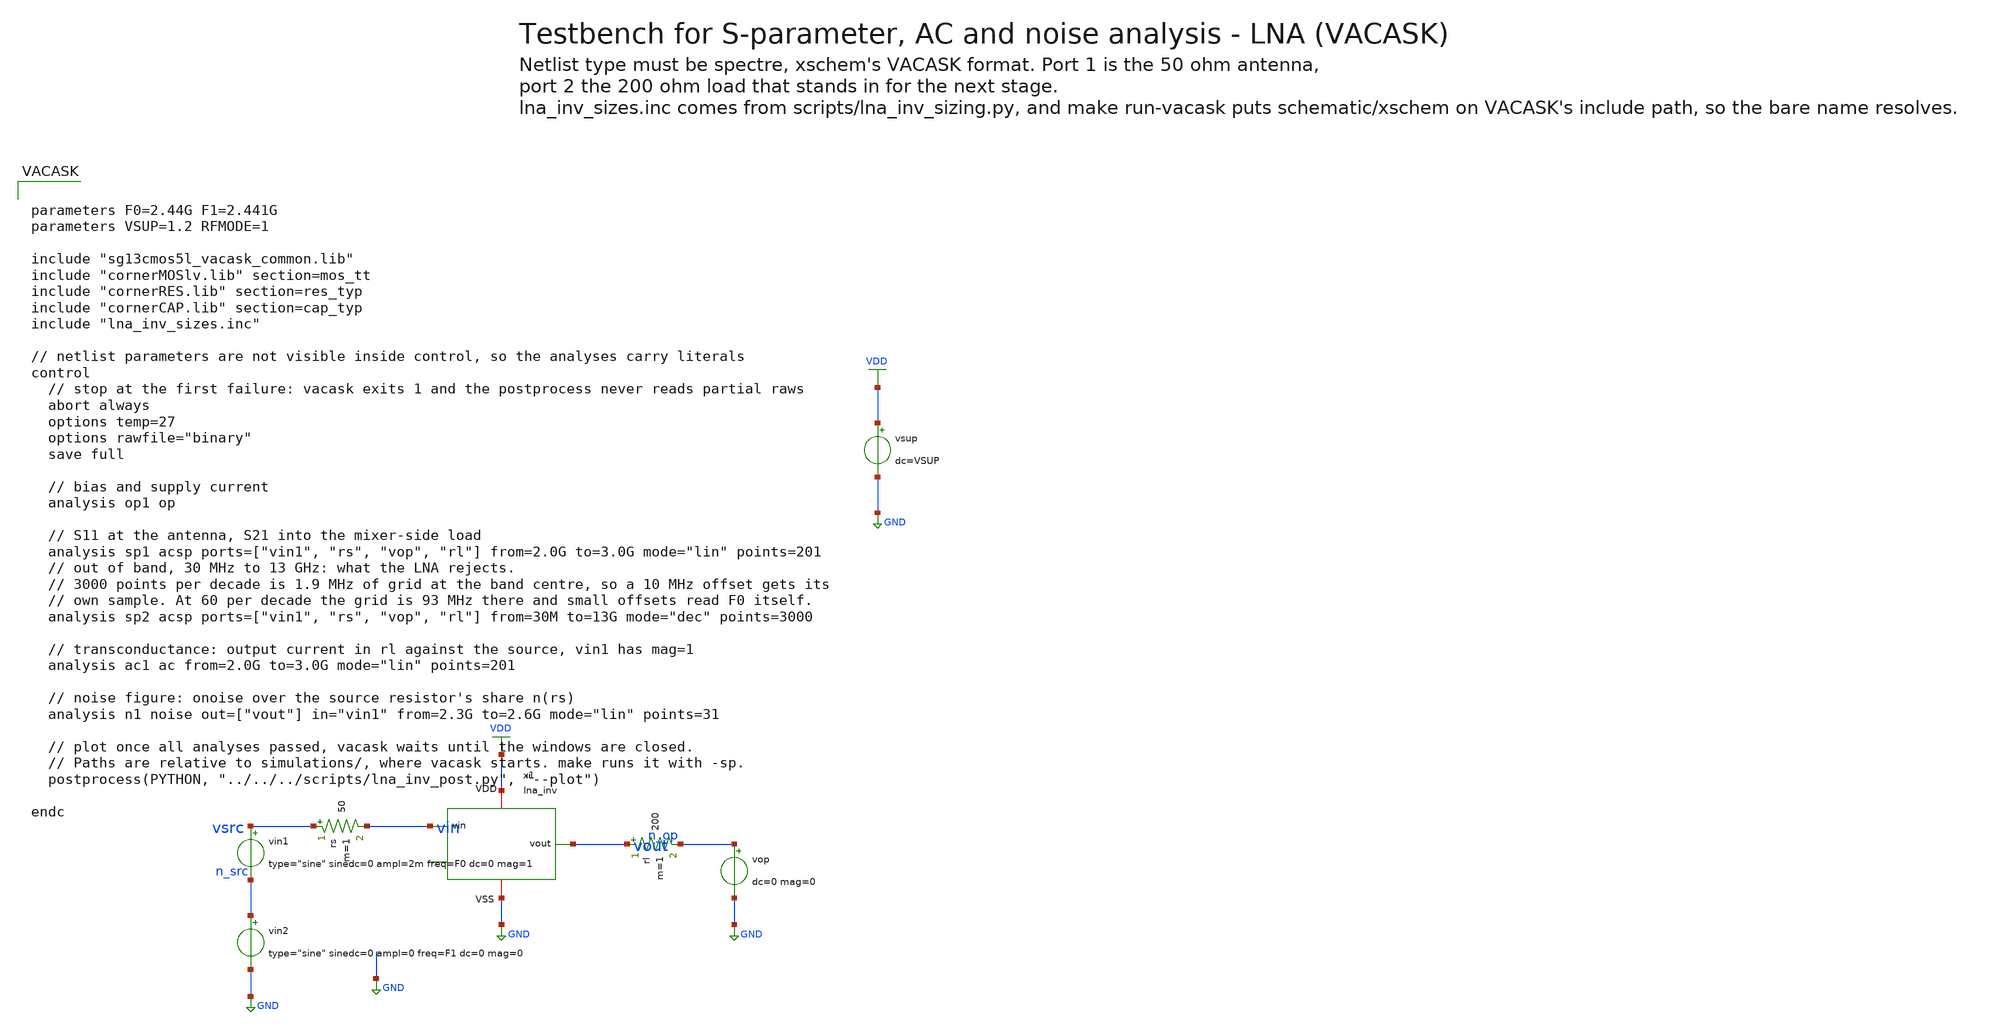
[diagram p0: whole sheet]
** sch_path: macros/lna_inv/testbenches/xschem/lna_inv_tb_sp.sch
**.subckt lna_inv_tb_sp
vin1 vsrc n_src type="sine" sinedc=0 ampl=2m freq=F0 dc=0 mag=1
vin2 n_src GND type="sine" sinedc=0 ampl=0 freq=F1 dc=0 mag=0
rs vsrc vin 50 m=1
x1 vin vout VDD GND lna_inv
rl vout n_op 200 m=1
vop n_op GND dc=0 mag=0
vsup VDD GND dc=VSUP
**** begin user architecture code


parameters F0=2.44G F1=2.441G
parameters VSUP=1.2 RFMODE=1

include "sg13cmos5l_vacask_common.lib"
include "cornerMOSlv.lib" section=mos_tt
include "cornerRES.lib" section=res_typ
include "cornerCAP.lib" section=cap_typ
include "lna_inv_sizes.inc"

// netlist parameters are not visible inside control, so the analyses carry literals
control
  // stop at the first failure: vacask exits 1 and the postprocess never reads partial raws
  abort always
  options temp=27
  options rawfile="binary"
  save full

  // bias and supply current
  analysis op1 op

  // S11 at the antenna, S21 into the mixer-side load
  analysis sp1 acsp ports=["vin1", "rs", "vop", "rl"] from=2.0G to=3.0G mode="lin" points=201
  // out of band, 30 MHz to 13 GHz: what the LNA rejects.
  // 3000 points per decade is 1.9 MHz of grid at the band centre, so a 10 MHz offset gets its
  // own sample. At 60 per decade the grid is 93 MHz there and small offsets read F0 itself.
  analysis sp2 acsp ports=["vin1", "rs", "vop", "rl"] from=30M to=13G mode="dec" points=3000

  // transconductance: output current in rl against the source, vin1 has mag=1
  analysis ac1 ac from=2.0G to=3.0G mode="lin" points=201

  // noise figure: onoise over the source resistor's share n(rs)
  analysis n1 noise out=["vout"] in="vin1" from=2.3G to=2.6G mode="lin" points=31

  // plot once all analyses passed, vacask waits until the windows are closed.
  // Paths are relative to simulations/, where vacask starts. make runs it with -sp.
  postprocess(PYTHON, "../../../scripts/lna_inv_post.py", "--plot")

endc


**** end user architecture code
**.ends
.GLOBAL GND
.GLOBAL VDD
.end
